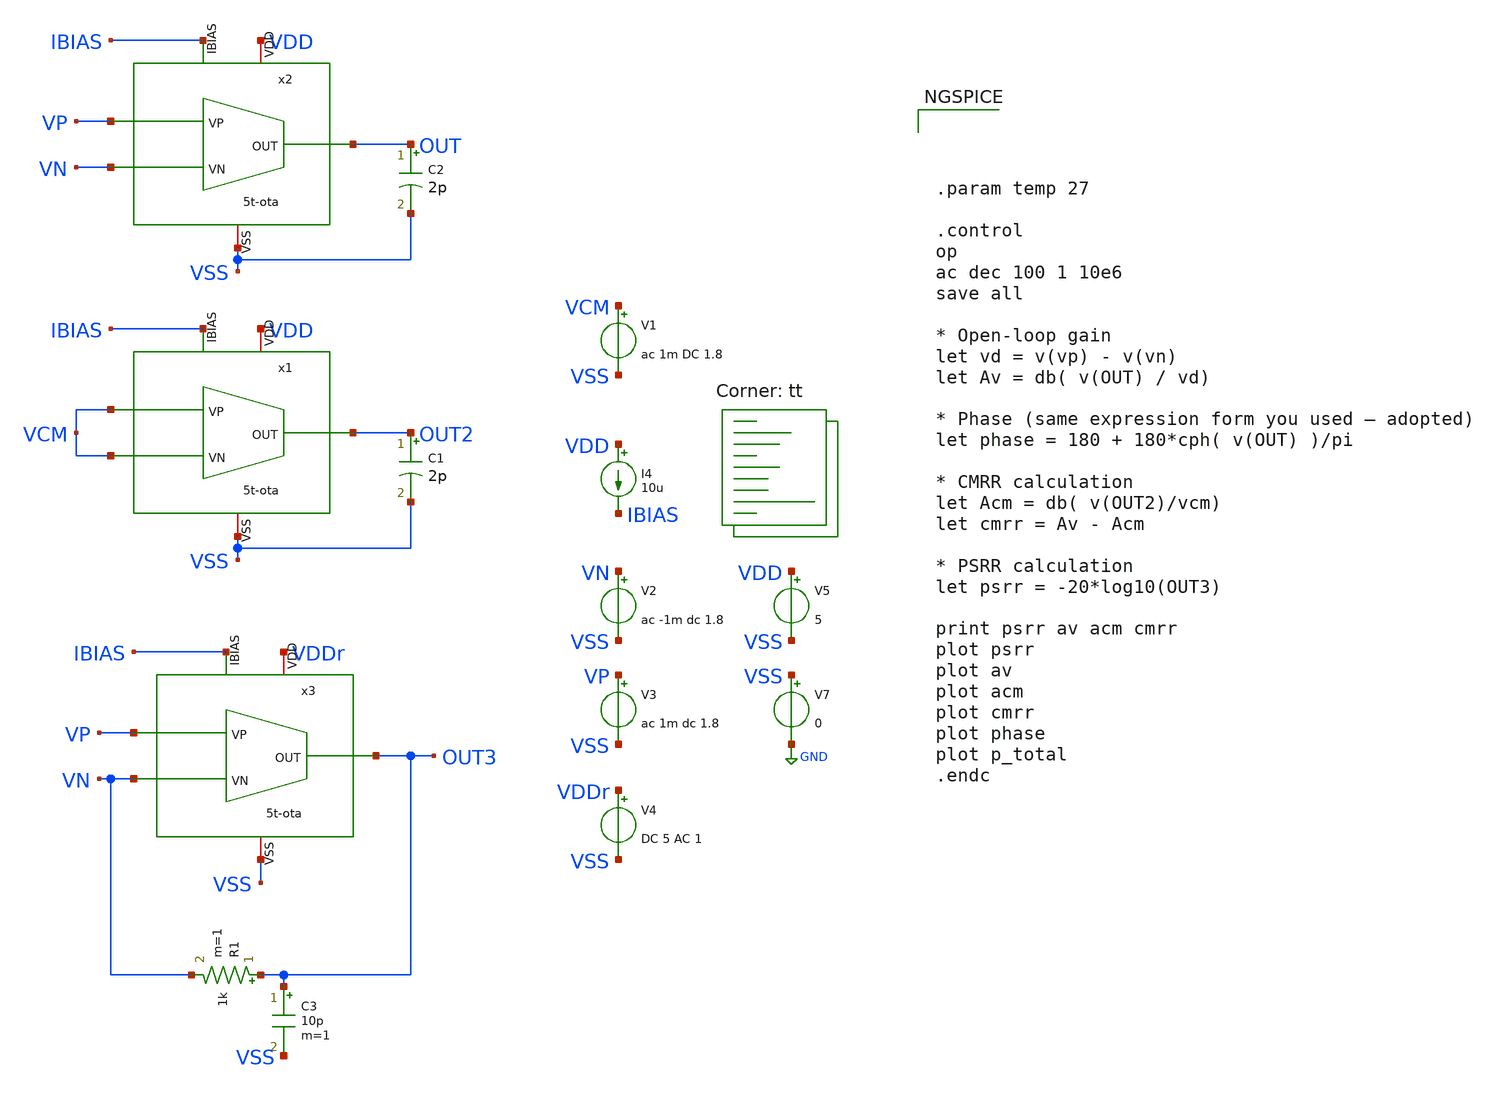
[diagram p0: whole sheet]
** sch_path: xschem/5t-ota/testbench/open-loop-gain.sch
**.subckt open-loop-gain
V2 VN VSS ac -1m dc 1.8
V3 VP VSS ac 1m dc 1.8
V5 VDD VSS 5
V7 VSS GND 0
C2 OUT VSS 2p m=1
x2 VDD OUT IBIAS VN VP VSS 5t-ota
I4 VDD IBIAS 10u
C1 OUT2 VSS 2p m=1
x1 VDD OUT2 IBIAS VCM VCM VSS 5t-ota
V1 VCM VSS ac 1m DC 1.8
x3 VDDr OUT3 IBIAS VN VP VSS 5t-ota
C3 OUT3 VSS 10p m=1
R1 OUT3 VN 1k m=1
V4 VDDr VSS DC 5 AC 1
**** begin user architecture code




.param temp 27

.control
op
ac dec 100 1 10e6
save all

* Open-loop gain
let vd = v(vp) - v(vn)
let Av = db( v(OUT) / vd)

* Phase (same expression form you used — adopted)
let phase = 180 + 180*cph( v(OUT) )/pi

* CMRR calculation
let Acm = db( v(OUT2)/vcm)
let cmrr = Av - Acm

* PSRR calculation
let psrr = -20*log10(OUT3)

print psrr av acm cmrr
plot psrr
plot av
plot acm
plot cmrr
plot phase
plot p_total
.endc



.lib $::SKYWATER_MODELS/sky130.lib.spice tt
**** end user architecture code
**.ends

* expanding   symbol:  icdec-biomedical-pmic/xschem/5t-ota/schematics/5t-ota.sym # of pins=6
** sym_path: xschem/5t-ota/schematics/5t-ota.sym
** sch_path: xschem/5t-ota/schematics/5t-ota.sch
.subckt 5t-ota VDD OUT IBIAS VN VP VSS
*.ipin VP
*.ipin VN
*.ipin IBIAS
*.iopin VDD
*.iopin VSS
*.opin OUT
XM1 net1 VP net2 VSS sky130_fd_pr__nfet_g5v0d10v5 L=0.75 W=8.5 nf=1 ad='int((nf+1)/2) * W/nf * 0.29'
+ as='int((nf+2)/2) * W/nf * 0.29' pd='2*int((nf+1)/2) * (W/nf + 0.29)' ps='2*int((nf+2)/2) * (W/nf + 0.29)'
+ nrd='0.29 / W' nrs='0.29 / W' sa=0 sb=0 sd=0 mult=1 m=1
XM2 OUT VN net2 VSS sky130_fd_pr__nfet_g5v0d10v5 L=0.75 W=8.5 nf=1 ad='int((nf+1)/2) * W/nf * 0.29' as='int((nf+2)/2) * W/nf * 0.29'
+ pd='2*int((nf+1)/2) * (W/nf + 0.29)' ps='2*int((nf+2)/2) * (W/nf + 0.29)' nrd='0.29 / W' nrs='0.29 / W'
+ sa=0 sb=0 sd=0 mult=1 m=1
XM3 net2 IBIAS VSS VSS sky130_fd_pr__nfet_g5v0d10v5 L=1.25 W=1.58 nf=1 ad='int((nf+1)/2) * W/nf * 0.29'
+ as='int((nf+2)/2) * W/nf * 0.29' pd='2*int((nf+1)/2) * (W/nf + 0.29)' ps='2*int((nf+2)/2) * (W/nf + 0.29)'
+ nrd='0.29 / W' nrs='0.29 / W' sa=0 sb=0 sd=0 mult=1 m=1
XM4 OUT net1 VDD VDD sky130_fd_pr__pfet_g5v0d10v5 L=1.25 W=4.85 nf=1 ad='int((nf+1)/2) * W/nf * 0.29'
+ as='int((nf+2)/2) * W/nf * 0.29' pd='2*int((nf+1)/2) * (W/nf + 0.29)' ps='2*int((nf+2)/2) * (W/nf + 0.29)'
+ nrd='0.29 / W' nrs='0.29 / W' sa=0 sb=0 sd=0 mult=1 m=1
XM5 net1 net1 VDD VDD sky130_fd_pr__pfet_g5v0d10v5 L=1.25 W=4.85 nf=1 ad='int((nf+1)/2) * W/nf * 0.29'
+ as='int((nf+2)/2) * W/nf * 0.29' pd='2*int((nf+1)/2) * (W/nf + 0.29)' ps='2*int((nf+2)/2) * (W/nf + 0.29)'
+ nrd='0.29 / W' nrs='0.29 / W' sa=0 sb=0 sd=0 mult=1 m=1
XM6 IBIAS IBIAS VSS VSS sky130_fd_pr__nfet_g5v0d10v5 L=1.25 W=1.58 nf=1 ad='int((nf+1)/2) * W/nf * 0.29'
+ as='int((nf+2)/2) * W/nf * 0.29' pd='2*int((nf+1)/2) * (W/nf + 0.29)' ps='2*int((nf+2)/2) * (W/nf + 0.29)'
+ nrd='0.29 / W' nrs='0.29 / W' sa=0 sb=0 sd=0 mult=1 m=1
.ends

.GLOBAL GND
.end
